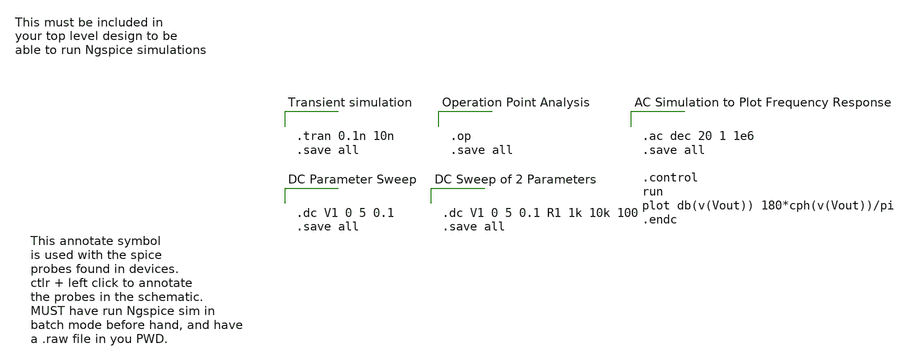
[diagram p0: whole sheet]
** sch_path: template/Analyses_Template.sch
**.subckt Analyses_Template
**** begin user architecture code
 .lib $::SKYWATER_MODELS/sky130.lib.spice tt
**** end user architecture code
**.ends
**** begin user architecture code


.dc V1 0 5 0.1
.save all




.ac dec 20 1 1e6
.save all

.control
run
plot db(v(Vout)) 180*cph(v(Vout))/pi
.endc




.dc V1 0 5 0.1 R1 1k 10k 100
.save all




.tran 0.1n 10n
.save all




.op
.save all


**** end user architecture code
.end
